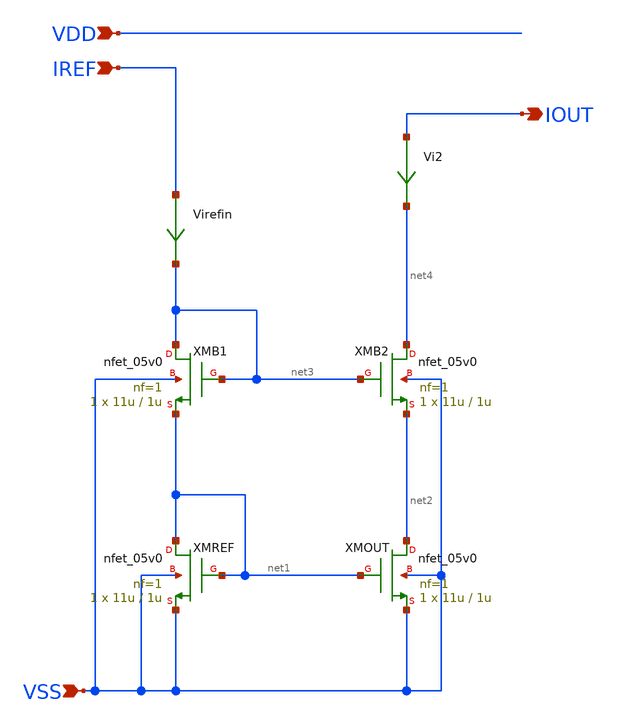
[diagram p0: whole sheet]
** sch_path: blocks/composite/regulated_cascoded_cmirror/Designs/design/cs-cascoded-cm.sch
**.subckt cs-cascoded-cm VDD VSS IREF IOUT
*.ipin VDD
*.ipin VSS
*.ipin IREF
*.opin IOUT
Virefin IREF net3 0
.save i(virefin)
XMREF net1 net1 VSS VSS nfet_05v0 L=1u W=11u nf=1 ad='int((nf+1)/2) * W/nf * 0.18u' as='int((nf+2)/2) * W/nf * 0.18u'
+ pd='2*int((nf+1)/2) * (W/nf + 0.18u)' ps='2*int((nf+2)/2) * (W/nf + 0.18u)' nrd='0.18u / W' nrs='0.18u / W'
+ sa=0 sb=0 sd=0 m=1
XMOUT net2 net1 VSS VSS nfet_05v0 L=1u W=11u nf=1 ad='int((nf+1)/2) * W/nf * 0.18u' as='int((nf+2)/2) * W/nf * 0.18u'
+ pd='2*int((nf+1)/2) * (W/nf + 0.18u)' ps='2*int((nf+2)/2) * (W/nf + 0.18u)' nrd='0.18u / W' nrs='0.18u / W'
+ sa=0 sb=0 sd=0 m=1
Vi2 IOUT net4 0
.save i(vi2)
XMB1 net3 net3 net1 VSS nfet_05v0 L=1u W=11u nf=1 ad='int((nf+1)/2) * W/nf * 0.18u' as='int((nf+2)/2) * W/nf * 0.18u'
+ pd='2*int((nf+1)/2) * (W/nf + 0.18u)' ps='2*int((nf+2)/2) * (W/nf + 0.18u)' nrd='0.18u / W' nrs='0.18u / W'
+ sa=0 sb=0 sd=0 m=1
XMB2 net4 net3 net2 VSS nfet_05v0 L=1u W=11u nf=1 ad='int((nf+1)/2) * W/nf * 0.18u' as='int((nf+2)/2) * W/nf * 0.18u'
+ pd='2*int((nf+1)/2) * (W/nf + 0.18u)' ps='2*int((nf+2)/2) * (W/nf + 0.18u)' nrd='0.18u / W' nrs='0.18u / W'
+ sa=0 sb=0 sd=0 m=1
**.ends
.end
